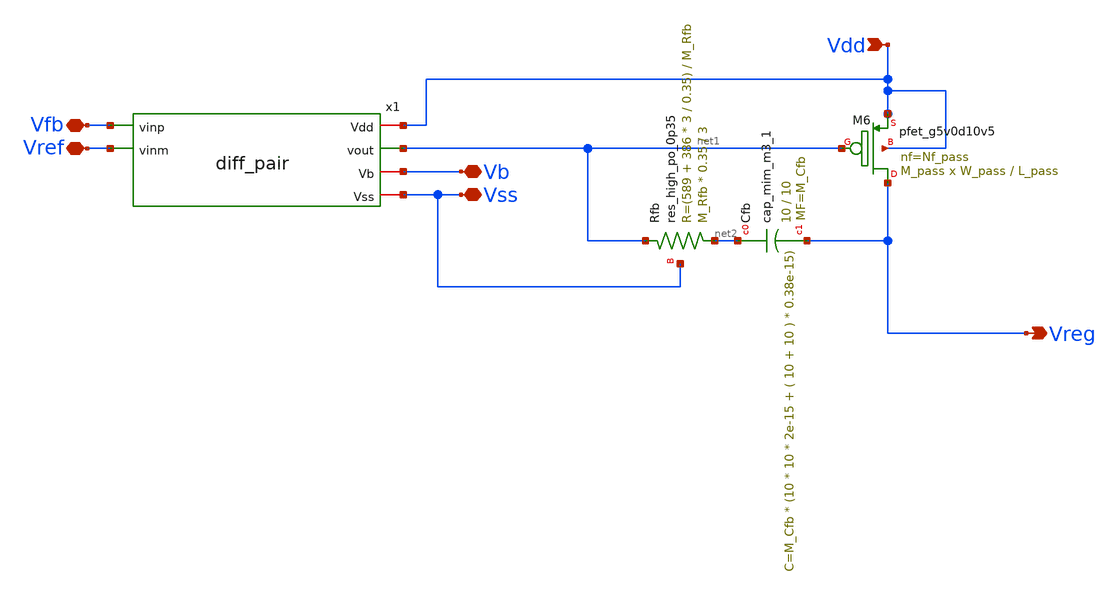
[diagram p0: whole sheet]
** sch_path: xschem/ldo.sch
**.subckt ldo Vb Vss Vreg Vref Vdd Vfb
*.iopin Vb
*.iopin Vss
*.opin Vreg
*.iopin Vref
*.ipin Vdd
*.iopin Vfb
x1 Vdd net1 Vfb Vref Vb Vss diff_pair
XM6 Vreg net1 Vdd Vdd sky130_fd_pr__pfet_g5v0d10v5 L=L_pass W=W_pass nf=Nf_pass ad='int((nf+1)/2) * W/nf * 0.29'
+ as='int((nf+2)/2) * W/nf * 0.29' pd='2*int((nf+1)/2) * (W/nf + 0.29)' ps='2*int((nf+2)/2) * (W/nf + 0.29)'
+ nrd='0.29 / W' nrs='0.29 / W' sa=0 sb=0 sd=0 mult=M_pass m=M_pass
XCfb net2 Vreg sky130_fd_pr__cap_mim_m3_1 W=10 L=10 MF=M_Cfb m=M_Cfb
XRfb net2 net1 Vss sky130_fd_pr__res_high_po_0p35 L=3 mult=M_Rfb m=M_Rfb
**.ends

* expanding   symbol:  diff_pair.sym # of pins=6
** sym_path: xschem/diff_pair.sym
** sch_path: xschem/diff_pair.sch
.subckt diff_pair Vdd vout vinp vinm Vb Vss
*.iopin Vdd
*.ipin vinm
*.ipin vinp
*.iopin Vb
*.opin vout
*.iopin Vss
XM1 net1 vinp net2 Vss sky130_fd_pr__nfet_g5v0d10v5 L=L_M1 W=W_M1 nf=1 ad='int((nf+1)/2) * W/nf * 0.29'
+ as='int((nf+2)/2) * W/nf * 0.29' pd='2*int((nf+1)/2) * (W/nf + 0.29)' ps='2*int((nf+2)/2) * (W/nf + 0.29)'
+ nrd='0.29 / W' nrs='0.29 / W' sa=0 sb=0 sd=0 mult=1 m=1
XM2 vout vinm net2 Vss sky130_fd_pr__nfet_g5v0d10v5 L=L_M2 W=W_M2 nf=1 ad='int((nf+1)/2) * W/nf * 0.29'
+ as='int((nf+2)/2) * W/nf * 0.29' pd='2*int((nf+1)/2) * (W/nf + 0.29)' ps='2*int((nf+2)/2) * (W/nf + 0.29)'
+ nrd='0.29 / W' nrs='0.29 / W' sa=0 sb=0 sd=0 mult=1 m=1
XM3 vout net1 Vdd Vdd sky130_fd_pr__pfet_g5v0d10v5 L=L_M3 W=W_M3 nf=1 ad='int((nf+1)/2) * W/nf * 0.29'
+ as='int((nf+2)/2) * W/nf * 0.29' pd='2*int((nf+1)/2) * (W/nf + 0.29)' ps='2*int((nf+2)/2) * (W/nf + 0.29)'
+ nrd='0.29 / W' nrs='0.29 / W' sa=0 sb=0 sd=0 mult=1 m=1
XM4 net1 net1 Vdd Vdd sky130_fd_pr__pfet_g5v0d10v5 L=L_M4 W=W_M4 nf=1 ad='int((nf+1)/2) * W/nf * 0.29'
+ as='int((nf+2)/2) * W/nf * 0.29' pd='2*int((nf+1)/2) * (W/nf + 0.29)' ps='2*int((nf+2)/2) * (W/nf + 0.29)'
+ nrd='0.29 / W' nrs='0.29 / W' sa=0 sb=0 sd=0 mult=1 m=1
XM5 net2 Vb Vss Vss sky130_fd_pr__nfet_g5v0d10v5 L=L_M5 W=W_M5 nf=1 ad='int((nf+1)/2) * W/nf * 0.29'
+ as='int((nf+2)/2) * W/nf * 0.29' pd='2*int((nf+1)/2) * (W/nf + 0.29)' ps='2*int((nf+2)/2) * (W/nf + 0.29)'
+ nrd='0.29 / W' nrs='0.29 / W' sa=0 sb=0 sd=0 mult=1 m=1
.ends

.end
